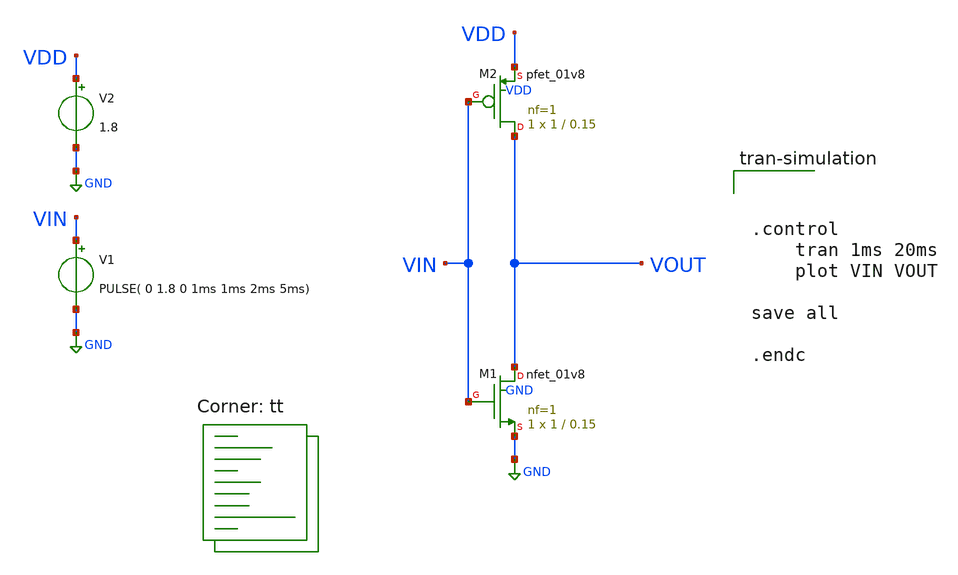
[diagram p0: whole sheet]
** sch_path: week01_mosfet_cmos/tugas3_simulasi_vtc/cmos-inv-tran.sch
**.subckt cmos-inv-tran
V1 VIN GND PULSE( 0 1.8 0 1ms 1ms 2ms 5ms)
V2 VDD GND 1.8
XM1 VOUT VIN GND GND sky130_fd_pr__nfet_01v8 L=0.15 W=1 nf=1 ad='int((nf+1)/2) * W/nf * 0.29' as='int((nf+2)/2) * W/nf * 0.29'
+ pd='2*int((nf+1)/2) * (W/nf + 0.29)' ps='2*int((nf+2)/2) * (W/nf + 0.29)' nrd='0.29 / W' nrs='0.29 / W'
+ sa=0 sb=0 sd=0 mult=1 m=1
XM2 VOUT VIN VDD VDD sky130_fd_pr__pfet_01v8 L=0.15 W=1 nf=1 ad='int((nf+1)/2) * W/nf * 0.29' as='int((nf+2)/2) * W/nf * 0.29'
+ pd='2*int((nf+1)/2) * (W/nf + 0.29)' ps='2*int((nf+2)/2) * (W/nf + 0.29)' nrd='0.29 / W' nrs='0.29 / W'
+ sa=0 sb=0 sd=0 mult=1 m=1
**** begin user architecture code
.lib $::SKYWATER_MODELS/sky130.lib.spice tt



.control
	tran 1ms 20ms
	plot VIN VOUT

save all

.endc


**** end user architecture code
**.ends
.GLOBAL GND
.end
